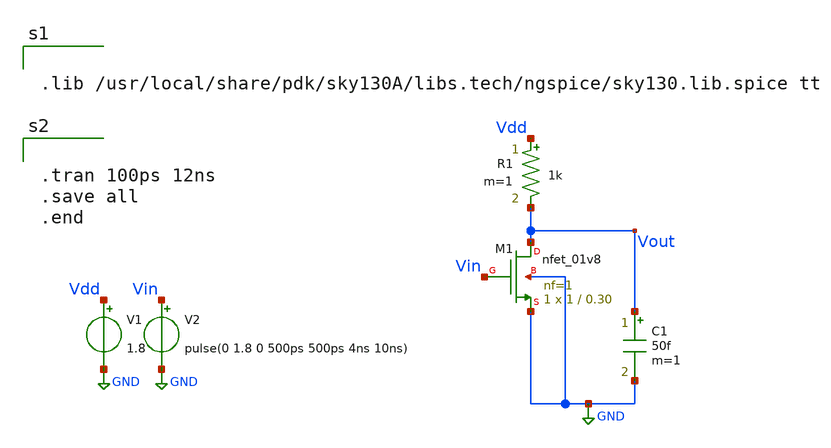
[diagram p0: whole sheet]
** sch_path: xschem files/nmos_as_inverter.sch
**.subckt nmos_as_inverter
R1 Vdd Vout 1k m=1
XM1 Vout Vin GND GND sky130_fd_pr__nfet_01v8 L=0.30 W=1 nf=1 ad='int((nf+1)/2) * W/nf * 0.29' as='int((nf+2)/2) * W/nf * 0.29'
+ pd='2*int((nf+1)/2) * (W/nf + 0.29)' ps='2*int((nf+2)/2) * (W/nf + 0.29)' nrd='0.29 / W' nrs='0.29 / W'
+ sa=0 sb=0 sd=0 mult=1 m=1
V1 Vdd GND 1.8
V2 Vin GND pulse(0 1.8 0 500ps 500ps 4ns 10ns)
C1 Vout GND 50f m=1
**** begin user architecture code


.lib /usr/local/share/pdk/sky130A/libs.tech/ngspice/sky130.lib.spice tt




.tran 100ps 12ns
.save all
.end


**** end user architecture code
**.ends
.GLOBAL GND
.end
